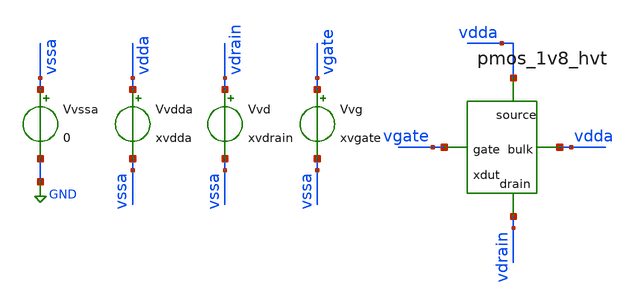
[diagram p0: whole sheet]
** sch_path: MC_analysis_across_corners/tb_mc_pmos.sch
**.subckt tb_mc_pmos
Vvdda vdda vssa xvdda
Vvssa vssa GND 0
Vvd vdrain vssa xvdrain
Vvg vgate vssa xvgate
xdut vdda vdda vgate vdrain pmos_1v8_hvt
**** begin user architecture code

** opencircuitdesign pdks install
*.lib $::SKYWATER_MODELS/sky130.lib.spice tt

.lib /home/slice/pdk/SW130/share/pdk/sky130A/libs.tech/combined/sky130.lib.spice tt_mm
*.lib /home/slice/pdk/SW130/share/pdk/sky130A/libs.tech/combined/sky130.lib.spice ss_mm
*.lib /home/slice/pdk/SW130/share/pdk/sky130A/libs.tech/combined/sky130.lib.spice sf_mm
*.lib /home/slice/pdk/SW130/share/pdk/sky130A/libs.tech/combined/sky130.lib.spice fs_mm
*.lib /home/slice/pdk/SW130/share/pdk/sky130A/libs.tech/combined/sky130.lib.spice ff_mm
*.lib /home/slice/pdk/SW130/share/pdk/sky130A/libs.tech/combined/sky130.lib.spice mc

*.lib /home/slice/pdk/SW130/share/pdk/sky130A/libs.tech/combined/sky130.lib.spice tt
*.lib /home/slice/pdk/SW130/share/pdk/sky130A/libs.tech/combined/sky130.lib.spice ss
*.lib /home/slice/pdk/SW130/share/pdk/sky130A/libs.tech/combined/sky130.lib.spice ff
*.lib /home/slice/pdk/SW130/share/pdk/sky130A/libs.tech/combined/sky130.lib.spice sf
*.lib /home/slice/pdk/SW130/share/pdk/sky130A/libs.tech/combined/sky130.lib.spice fs

* Parameters
.param xvdda = 1.8
.csparam xvdda_var = 'xvdda'
.param xvdrain = 1
.param xvgate = 1
.temp 27

  ** 1. DCOP analysis **
  ** must save the below for DCOP analysis to be back annotated onto the schematic
  .option savecurrents
  .save

  * svt device
  +  @m.xdut.xm1.msky130_fd_pr__pfet_01v8[vgs]
  +  @m.xdut.xm1.msky130_fd_pr__pfet_01v8[vds]
  +  @m.xdut.xm1.msky130_fd_pr__pfet_01v8[vth]
  +  @m.xdut.xm1.msky130_fd_pr__pfet_01v8[gds]
  +  @m.xdut.xm1.msky130_fd_pr__pfet_01v8[gm]
  +  @m.xdut.xm1.msky130_fd_pr__pfet_01v8[id]
  +  @m.xdut.xm1.msky130_fd_pr__pfet_01v8[vdsat]
  * hvt device
  +  @m.xdut.xm1.msky130_fd_pr__pfet_01v8_hvt[vgs]
  +  @m.xdut.xm1.msky130_fd_pr__pfet_01v8_hvt[vds]
  +  @m.xdut.xm1.msky130_fd_pr__pfet_01v8_hvt[vth]
  +  @m.xdut.xm1.msky130_fd_pr__pfet_01v8_hvt[gds]
  +  @m.xdut.xm1.msky130_fd_pr__pfet_01v8_hvt[gm]
  +  @m.xdut.xm1.msky130_fd_pr__pfet_01v8_hvt[id]
  +  @m.xdut.xm1.msky130_fd_pr__pfet_01v8_hvt[vdsat]
  * lvt device
  +  @m.xdut.xm1.msky130_fd_pr__pfet_01v8_lvt[vgs]
  +  @m.xdut.xm1.msky130_fd_pr__pfet_01v8_lvt[vds]
  +  @m.xdut.xm1.msky130_fd_pr__pfet_01v8_lvt[vth]
  +  @m.xdut.xm1.msky130_fd_pr__pfet_01v8_lvt[gds]
  +  @m.xdut.xm1.msky130_fd_pr__pfet_01v8_lvt[gm]
  +  @m.xdut.xm1.msky130_fd_pr__pfet_01v8_lvt[id]
  +  @m.xdut.xm1.msky130_fd_pr__pfet_01v8_lvt[vdsat]

  .control


    save all

    let run = 1
    let cor_id = 1
    echo "$&cor_id" >> vth_measures_tt_mm.txt

    dowhile run <= 200
    reset

    ** 1. DCOP ANALYSIS **
    op
    *let vth_meas = @m.xdut.xm1.msky130_fd_pr__pfet_01v8[vth]
    *let vth_meas = @m.xdut.xm1.msky130_fd_pr__pfet_01v8_lvt[vth]
    let vth_meas = @m.xdut.xm1.msky130_fd_pr__pfet_01v8_hvt[vth]
    *echo "$&vth_meas" >> vth_measures_all_mm.txt
    echo "$&vth_meas" >> vth_measures_tt_mm.txt
    remzerovec
    * need to set appendwrite to accumulate the vth's from all runs
    * in one file. THIS MEANS YOU MUST ENSURE FILE "vth_measures.txt" IS
    * DELETED FROM THE RUNDIR PRIOR TO RUNNING THIS LOOP. Otherwise
    * MC data from an older analysis will corrupt the results from your
    * current analysis. For best practice you should also delete file
    * "tb_MC_PMOS.raw" to save diskspace.
    *set appendwrite
    *set filetype=ascii
    *write tb_MC_PMOS.raw
    * release the memory holding the output data sets (good memory management)
    destroy all
    let run = run+1
    end

  setplot

quit 0
.endc




**** end user architecture code
**.ends

* expanding   symbol:  pmos_1v8_hvt.sym # of pins=4
** sym_path: MC_analysis_across_corners/DUT.sym
** sch_path: MC_analysis_across_corners/pmos_1v8_hvt.sch
.subckt pmos_1v8_hvt source bulk gate drain
*.ipin gate
*.ipin source
*.ipin bulk
*.opin drain
XM1 drain gate source bulk sky130_fd_pr__pfet_01v8_hvt L=2 W=1 nf=1 ad='int((nf+1)/2) * W/nf * 0.29' as='int((nf+2)/2)
+ * W/nf * 0.29' pd='2*int((nf+1)/2) * (W/nf + 0.29)' ps='2*int((nf+2)/2) * (W/nf + 0.29)' nrd='0.29 /
+ W' nrs='0.29 / W' sa=0 sb=0 sd=0 mult=1 m=1
.ends

.GLOBAL GND
.end
